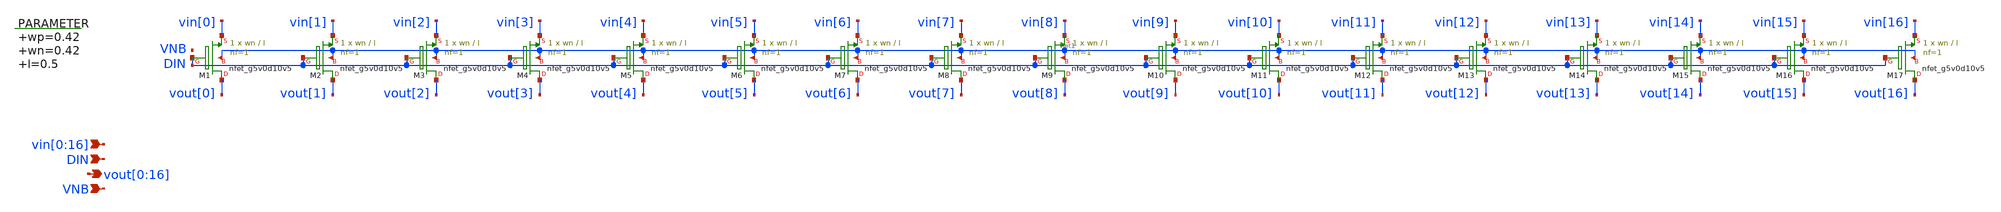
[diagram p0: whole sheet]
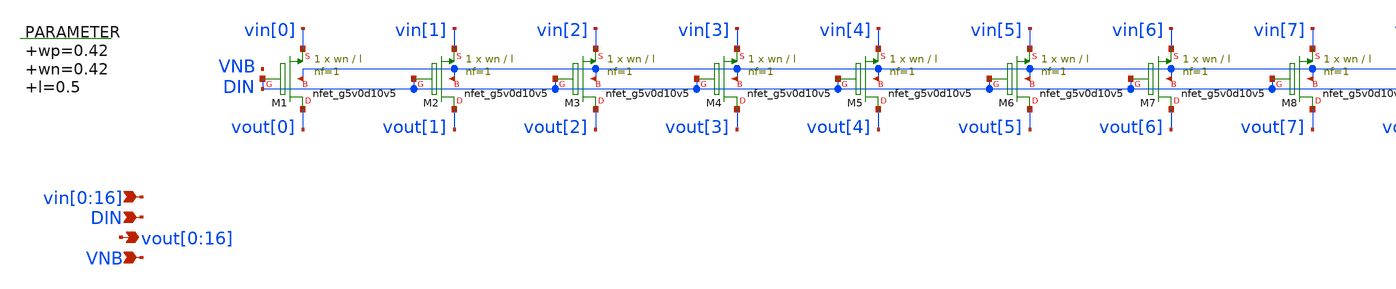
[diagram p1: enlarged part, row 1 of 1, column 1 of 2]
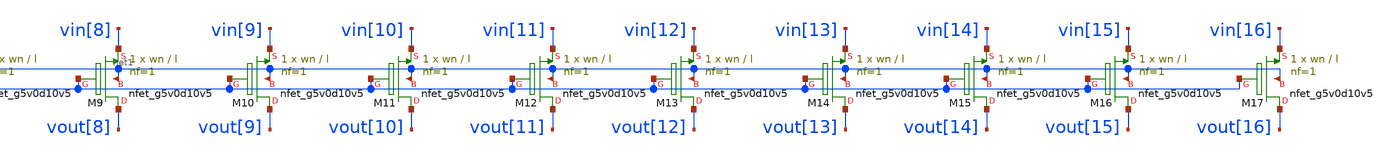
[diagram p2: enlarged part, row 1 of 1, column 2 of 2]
** sch_path: xschem/vselector_16b.sch
**.subckt vselector_16b
*+ vin[0],vin[1],vin[2],vin[3],vin[4],vin[5],vin[6],vin[7],vin[8],vin[9],vin[10],vin[11],vin[12],vin[13],vin[14],vin[15],vin[16]
*+ vout[0],vout[1],vout[2],vout[3],vout[4],vout[5],vout[6],vout[7],vout[8],vout[9],vout[10],vout[11],vout[12],vout[13],vout[14],vout[15],vout[16] VNB DIN
*.ipin
*+ vin[0],vin[1],vin[2],vin[3],vin[4],vin[5],vin[6],vin[7],vin[8],vin[9],vin[10],vin[11],vin[12],vin[13],vin[14],vin[15],vin[16]
*.opin
*+ vout[0],vout[1],vout[2],vout[3],vout[4],vout[5],vout[6],vout[7],vout[8],vout[9],vout[10],vout[11],vout[12],vout[13],vout[14],vout[15],vout[16]
*.ipin VNB
*.ipin DIN
.param wp=0.42 wn=0.42 l=0.5

XM1 vout[0] DIN vin[0] net1 sky130_fd_pr__nfet_g5v0d10v5 L=l W=wn nf=1 ad='int((nf+1)/2) * W/nf * 0.29'
+ as='int((nf+2)/2) * W/nf * 0.29' pd='2*int((nf+1)/2) * (W/nf + 0.29)' ps='2*int((nf+2)/2) * (W/nf + 0.29)'
+ nrd='0.29 / W' nrs='0.29 / W' sa=0 sb=0 sd=0 mult=1 m=1
XM2 vout[1] DIN vin[1] net1 sky130_fd_pr__nfet_g5v0d10v5 L=l W=wn nf=1 ad='int((nf+1)/2) * W/nf * 0.29'
+ as='int((nf+2)/2) * W/nf * 0.29' pd='2*int((nf+1)/2) * (W/nf + 0.29)' ps='2*int((nf+2)/2) * (W/nf + 0.29)'
+ nrd='0.29 / W' nrs='0.29 / W' sa=0 sb=0 sd=0 mult=1 m=1
XM3 vout[2] DIN vin[2] net1 sky130_fd_pr__nfet_g5v0d10v5 L=l W=wn nf=1 ad='int((nf+1)/2) * W/nf * 0.29'
+ as='int((nf+2)/2) * W/nf * 0.29' pd='2*int((nf+1)/2) * (W/nf + 0.29)' ps='2*int((nf+2)/2) * (W/nf + 0.29)'
+ nrd='0.29 / W' nrs='0.29 / W' sa=0 sb=0 sd=0 mult=1 m=1
XM4 vout[3] DIN vin[3] net1 sky130_fd_pr__nfet_g5v0d10v5 L=l W=wn nf=1 ad='int((nf+1)/2) * W/nf * 0.29'
+ as='int((nf+2)/2) * W/nf * 0.29' pd='2*int((nf+1)/2) * (W/nf + 0.29)' ps='2*int((nf+2)/2) * (W/nf + 0.29)'
+ nrd='0.29 / W' nrs='0.29 / W' sa=0 sb=0 sd=0 mult=1 m=1
XM5 vout[4] DIN vin[4] net1 sky130_fd_pr__nfet_g5v0d10v5 L=l W=wn nf=1 ad='int((nf+1)/2) * W/nf * 0.29'
+ as='int((nf+2)/2) * W/nf * 0.29' pd='2*int((nf+1)/2) * (W/nf + 0.29)' ps='2*int((nf+2)/2) * (W/nf + 0.29)'
+ nrd='0.29 / W' nrs='0.29 / W' sa=0 sb=0 sd=0 mult=1 m=1
XM6 vout[5] DIN vin[5] net1 sky130_fd_pr__nfet_g5v0d10v5 L=l W=wn nf=1 ad='int((nf+1)/2) * W/nf * 0.29'
+ as='int((nf+2)/2) * W/nf * 0.29' pd='2*int((nf+1)/2) * (W/nf + 0.29)' ps='2*int((nf+2)/2) * (W/nf + 0.29)'
+ nrd='0.29 / W' nrs='0.29 / W' sa=0 sb=0 sd=0 mult=1 m=1
XM7 vout[6] DIN vin[6] net1 sky130_fd_pr__nfet_g5v0d10v5 L=l W=wn nf=1 ad='int((nf+1)/2) * W/nf * 0.29'
+ as='int((nf+2)/2) * W/nf * 0.29' pd='2*int((nf+1)/2) * (W/nf + 0.29)' ps='2*int((nf+2)/2) * (W/nf + 0.29)'
+ nrd='0.29 / W' nrs='0.29 / W' sa=0 sb=0 sd=0 mult=1 m=1
XM8 vout[7] DIN vin[7] net1 sky130_fd_pr__nfet_g5v0d10v5 L=l W=wn nf=1 ad='int((nf+1)/2) * W/nf * 0.29'
+ as='int((nf+2)/2) * W/nf * 0.29' pd='2*int((nf+1)/2) * (W/nf + 0.29)' ps='2*int((nf+2)/2) * (W/nf + 0.29)'
+ nrd='0.29 / W' nrs='0.29 / W' sa=0 sb=0 sd=0 mult=1 m=1
XM9 vout[8] DIN vin[8] net1 sky130_fd_pr__nfet_g5v0d10v5 L=l W=wn nf=1 ad='int((nf+1)/2) * W/nf * 0.29'
+ as='int((nf+2)/2) * W/nf * 0.29' pd='2*int((nf+1)/2) * (W/nf + 0.29)' ps='2*int((nf+2)/2) * (W/nf + 0.29)'
+ nrd='0.29 / W' nrs='0.29 / W' sa=0 sb=0 sd=0 mult=1 m=1
XM10 vout[9] DIN vin[9] net1 sky130_fd_pr__nfet_g5v0d10v5 L=l W=wn nf=1 ad='int((nf+1)/2) * W/nf * 0.29'
+ as='int((nf+2)/2) * W/nf * 0.29' pd='2*int((nf+1)/2) * (W/nf + 0.29)' ps='2*int((nf+2)/2) * (W/nf + 0.29)'
+ nrd='0.29 / W' nrs='0.29 / W' sa=0 sb=0 sd=0 mult=1 m=1
XM11 vout[10] DIN vin[10] net1 sky130_fd_pr__nfet_g5v0d10v5 L=l W=wn nf=1 ad='int((nf+1)/2) * W/nf * 0.29'
+ as='int((nf+2)/2) * W/nf * 0.29' pd='2*int((nf+1)/2) * (W/nf + 0.29)' ps='2*int((nf+2)/2) * (W/nf + 0.29)'
+ nrd='0.29 / W' nrs='0.29 / W' sa=0 sb=0 sd=0 mult=1 m=1
XM12 vout[11] DIN vin[11] net1 sky130_fd_pr__nfet_g5v0d10v5 L=l W=wn nf=1 ad='int((nf+1)/2) * W/nf * 0.29'
+ as='int((nf+2)/2) * W/nf * 0.29' pd='2*int((nf+1)/2) * (W/nf + 0.29)' ps='2*int((nf+2)/2) * (W/nf + 0.29)'
+ nrd='0.29 / W' nrs='0.29 / W' sa=0 sb=0 sd=0 mult=1 m=1
XM13 vout[12] DIN vin[12] net1 sky130_fd_pr__nfet_g5v0d10v5 L=l W=wn nf=1 ad='int((nf+1)/2) * W/nf * 0.29'
+ as='int((nf+2)/2) * W/nf * 0.29' pd='2*int((nf+1)/2) * (W/nf + 0.29)' ps='2*int((nf+2)/2) * (W/nf + 0.29)'
+ nrd='0.29 / W' nrs='0.29 / W' sa=0 sb=0 sd=0 mult=1 m=1
XM14 vout[13] DIN vin[13] net1 sky130_fd_pr__nfet_g5v0d10v5 L=l W=wn nf=1 ad='int((nf+1)/2) * W/nf * 0.29'
+ as='int((nf+2)/2) * W/nf * 0.29' pd='2*int((nf+1)/2) * (W/nf + 0.29)' ps='2*int((nf+2)/2) * (W/nf + 0.29)'
+ nrd='0.29 / W' nrs='0.29 / W' sa=0 sb=0 sd=0 mult=1 m=1
XM15 vout[14] DIN vin[14] net1 sky130_fd_pr__nfet_g5v0d10v5 L=l W=wn nf=1 ad='int((nf+1)/2) * W/nf * 0.29'
+ as='int((nf+2)/2) * W/nf * 0.29' pd='2*int((nf+1)/2) * (W/nf + 0.29)' ps='2*int((nf+2)/2) * (W/nf + 0.29)'
+ nrd='0.29 / W' nrs='0.29 / W' sa=0 sb=0 sd=0 mult=1 m=1
XM16 vout[15] DIN vin[15] net1 sky130_fd_pr__nfet_g5v0d10v5 L=l W=wn nf=1 ad='int((nf+1)/2) * W/nf * 0.29'
+ as='int((nf+2)/2) * W/nf * 0.29' pd='2*int((nf+1)/2) * (W/nf + 0.29)' ps='2*int((nf+2)/2) * (W/nf + 0.29)'
+ nrd='0.29 / W' nrs='0.29 / W' sa=0 sb=0 sd=0 mult=1 m=1
XM17 vout[16] DIN vin[16] net1 sky130_fd_pr__nfet_g5v0d10v5 L=l W=wn nf=1 ad='int((nf+1)/2) * W/nf * 0.29'
+ as='int((nf+2)/2) * W/nf * 0.29' pd='2*int((nf+1)/2) * (W/nf + 0.29)' ps='2*int((nf+2)/2) * (W/nf + 0.29)'
+ nrd='0.29 / W' nrs='0.29 / W' sa=0 sb=0 sd=0 mult=1 m=1
**.ends
.end
